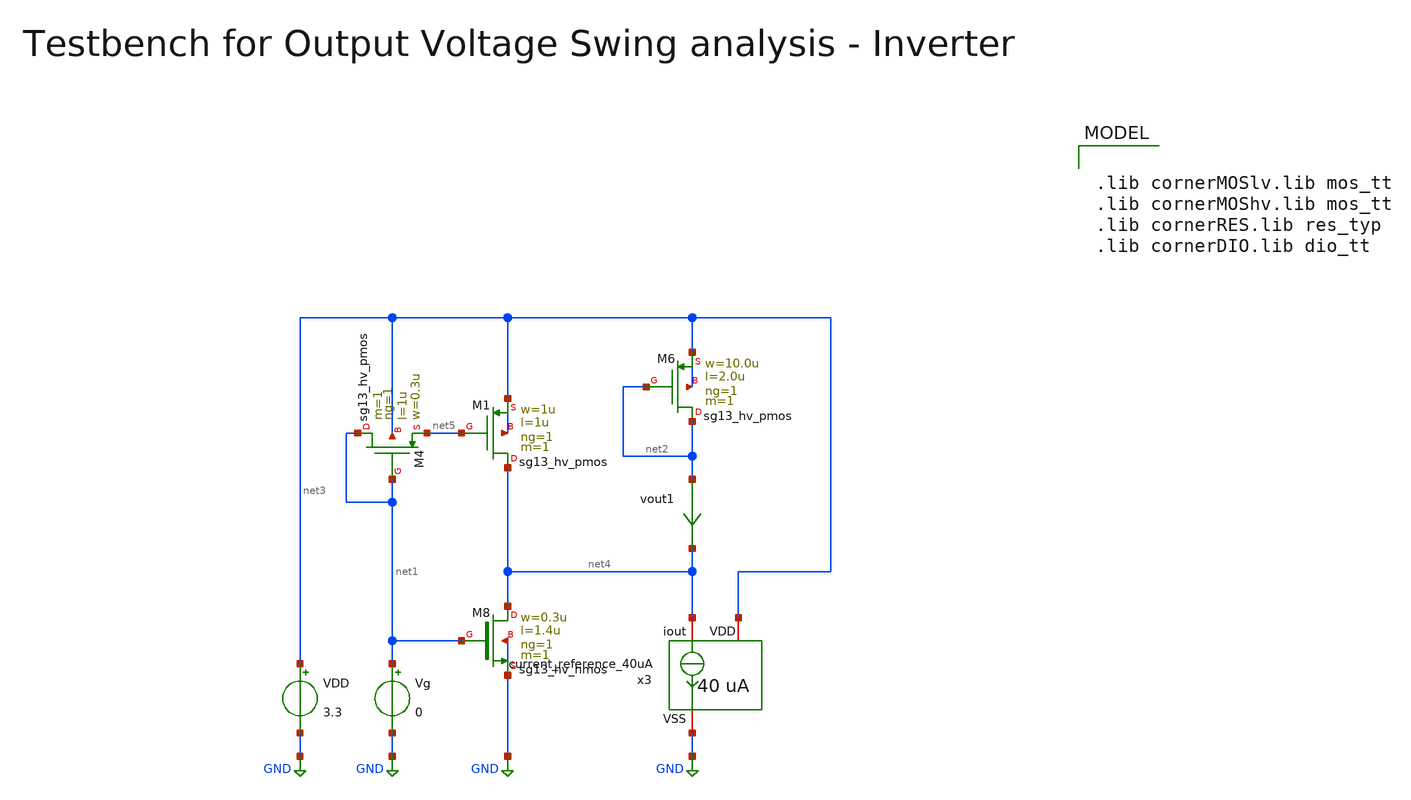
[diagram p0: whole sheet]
** sch_path: macros/heichips26_vcr/macros/switched_capacitor/testbenches/xschem/tb_v-to-i_dc.sch
**.subckt tb_v-to-i_dc
VDD net3 GND 3.3
Vg net1 GND 0
vout1 net2 net4 0
.save i(vout1)
XM8 net4 net1 GND GND sg13_hv_nmos w=0.3u l=1.4u ng=1 m=1 mm_ok=1
XM6 net2 net2 net3 net3 sg13_hv_pmos w=10.0u l=2.0u ng=1 m=1 mm_ok=1
XM1 net4 net5 net3 net3 sg13_hv_pmos w=1u l=1u ng=1 m=1 mm_ok=1
XM4 net1 net1 net5 net3 sg13_hv_pmos w=0.3u l=1u ng=1 m=1 mm_ok=1
x3 net3 net4 GND current_reference_40uA
**** begin user architecture code


.include ../../../netlist/pex/inverter_magic_pex_3.spice
.param temp=27
.options savecurrents klu method=gear reltol=1e-3 abstol=1e-15 gmin=1e-15
.control

save all

* Operating Point Analysis
op
remzerovec
write @schname\.raw
set appendwrite

* DC Sweep
dc Vg 3.3 0 -0.01
remzerovec
write @schname\.raw
set appendwrite

* Plotting
plot i(vout1)
plot deriv(i(vout1)) mean(deriv(i(vout1)))
plot i(VDD)
*plot vin

* Measurement
*meas dc Vgsp_at_Vcm when vout=Vcm
*print Vgsp_at_Vcm

* Write Data
*unset appendwrite
*set wr_vecnames
*set wr_singlescale
*wrdata ../plot_simulations/data/@schname\.txt v(vin) v(vout)

*quit
.endc



.lib cornerMOSlv.lib mos_tt
.lib cornerMOShv.lib mos_tt
.lib cornerRES.lib res_typ
.lib cornerDIO.lib dio_tt

**** end user architecture code
**.ends

* expanding   symbol:  current_reference_40uA.sym # of pins=3
** sym_path: macros/heichips26_vcr/macros/switched_capacitor/schematic/xschem/current_reference_40uA.sym
** sch_path: macros/heichips26_vcr/macros/switched_capacitor/schematic/xschem/current_reference_40uA.sch
.subckt current_reference_40uA VDD iout VSS
*.iopin VSS
*.iopin VDD
*.iopin iout
XM8 net2 net2 VSS VSS sg13_hv_nmos w=n_w l=n_l ng=1 m=1 mm_ok=1
XM6 net2 net1 VDD VDD sg13_hv_pmos w=p_w l=p_l ng=1 m=1 mm_ok=1
XM1 net1 net1 VDD VDD sg13_hv_pmos w=p_w l=p_l ng=1 m=1 mm_ok=1
XM3 net1 net2 net3 VSS sg13_hv_nmos w=n_w l=n_l ng=1 m=1 mm_ok=1
XR2 net3 net4 VSS rppd w=2e-6 l=21.9e-6 m=1 b=0 mm_ok=1
XM2 net1 net2 net3 VSS sg13_hv_nmos w=n_w l=n_l ng=1 m=1 mm_ok=1
XM4 net1 net2 net3 VSS sg13_hv_nmos w=n_w l=n_l ng=1 m=1 mm_ok=1
XM5 net1 net2 net3 VSS sg13_hv_nmos w=n_w l=n_l ng=1 m=1 mm_ok=1
XM7 iout net2 VSS VSS sg13_hv_nmos w=n_w l=n_l ng=1 m=1 mm_ok=1
XR3 net4 VSS VSS rsil w=0.5e-6 l=365e-6 m=1 mm_ok=1
**** begin user architecture code


.param n_w = 6u
.param n_l = 5u
.param p_w = 10u
.param p_l = 2u


**** end user architecture code
.ends

.GLOBAL GND
.end
